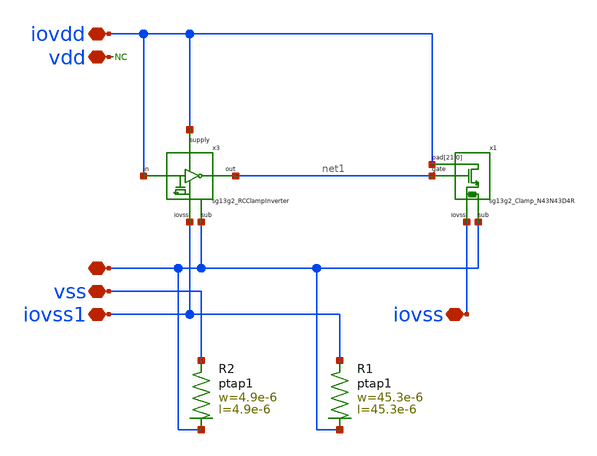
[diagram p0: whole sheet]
** sch_path: MSPHY6034-main/dependencies/unic_cass_2025_team04_padring/xschem/openpdk-libraries/ihp-sg13g2/sg13g2_io/xschem/sg13g2_IOPadIOVdd.sch
**.subckt sg13g2_IOPadIOVdd iovdd vss vdd ! iovss1 iovss
*.iopin iovdd
*.iopin vss
*.iopin vdd
*.iopin !
*.iopin iovss1
*.iopin iovss
XR2 vss ! ptap1 R=22.47 w=4.9e-6 l=4.9e-6
* noconn vdd
XR1 iovss1 ! ptap1 R=438.8m w=45.3e-6 l=45.3e-6
x1 iovss iovdd iovdd iovdd iovdd iovdd iovdd iovdd iovdd iovdd iovdd iovdd iovdd iovdd iovdd iovdd
+ iovdd iovdd iovdd iovdd iovdd iovdd iovdd ! net1 sg13g2_Clamp_N43N43D4R
x3 iovdd iovss1 iovdd net1 ! sg13g2_RCClampInverter
**.ends

* expanding   symbol:  sg13g2_Clamp_N43N43D4R.sym # of pins=4
** sym_path: MSPHY6034-main/schematic/xschem/openpdk-libraries/ihp-sg13g2/sg13g2_io/xschem/sg13g2_Clamp_N43N43D4R.sym
** sch_path: MSPHY6034-main/schematic/xschem/openpdk-libraries/ihp-sg13g2/sg13g2_io/xschem/sg13g2_Clamp_N43N43D4R.sch
.subckt sg13g2_Clamp_N43N43D4R iovss pad[21] pad[20] pad[19] pad[18] pad[17] pad[16] pad[15] pad[14]
+ pad[13] pad[12] pad[11] pad[10] pad[9] pad[8] pad[7] pad[6] pad[5] pad[4] pad[3] pad[2] pad[1] pad[0] sub
+ gate
*.iopin iovss
*.iopin
*+ pad[21],pad[20],pad[19],pad[18],pad[17],pad[16],pad[15],pad[14],pad[13],pad[12],pad[11],pad[10],pad[9],pad[8],pad[7],pad[6],pad[5],pad[4],pad[3],pad[2],pad[1],pad[0]
*.iopin sub
*.iopin gate
XR1 iovss sub ptap1 R=9.999 w=8.1e-6 l=8.1e-6
XM1 pad[11] gate iovss sub sg13_hv_nmos w=35.2u l=0.6u ng=8 m=1 mm_ok=1
XM2 pad[12] gate iovss sub sg13_hv_nmos w=35.2u l=0.6u ng=8 m=1 mm_ok=1
XM3 pad[13] gate iovss sub sg13_hv_nmos w=35.2u l=0.6u ng=8 m=1 mm_ok=1
XM4 pad[14] gate iovss sub sg13_hv_nmos w=35.2u l=0.6u ng=8 m=1 mm_ok=1
XM5 pad[15] gate iovss sub sg13_hv_nmos w=35.2u l=0.6u ng=8 m=1 mm_ok=1
XM6 pad[16] gate iovss sub sg13_hv_nmos w=35.2u l=0.6u ng=8 m=1 mm_ok=1
XM7 pad[17] gate iovss sub sg13_hv_nmos w=35.2u l=0.6u ng=8 m=1 mm_ok=1
XM8 pad[18] gate iovss sub sg13_hv_nmos w=35.2u l=0.6u ng=8 m=1 mm_ok=1
XM9 pad[19] gate iovss sub sg13_hv_nmos w=35.2u l=0.6u ng=8 m=1 mm_ok=1
XM10 pad[20] gate iovss sub sg13_hv_nmos w=35.2u l=0.6u ng=8 m=1 mm_ok=1
XM11 pad[21] gate iovss sub sg13_hv_nmos w=17.6u l=0.6u ng=4 m=1 mm_ok=1
XD1 sub gate dantenna l=0.48u w=0.48u
XM12 pad[0] gate iovss sub sg13_hv_nmos w=35.2u l=0.6u ng=8 m=1 mm_ok=1
XM13 pad[1] gate iovss sub sg13_hv_nmos w=35.2u l=0.6u ng=8 m=1 mm_ok=1
XM14 pad[2] gate iovss sub sg13_hv_nmos w=35.2u l=0.6u ng=8 m=1 mm_ok=1
XM15 pad[3] gate iovss sub sg13_hv_nmos w=35.2u l=0.6u ng=8 m=1 mm_ok=1
XM16 pad[4] gate iovss sub sg13_hv_nmos w=35.2u l=0.6u ng=8 m=1 mm_ok=1
XM17 pad[5] gate iovss sub sg13_hv_nmos w=35.2u l=0.6u ng=8 m=1 mm_ok=1
XM18 pad[6] gate iovss sub sg13_hv_nmos w=35.2u l=0.6u ng=8 m=1 mm_ok=1
XM19 pad[7] gate iovss sub sg13_hv_nmos w=35.2u l=0.6u ng=8 m=1 mm_ok=1
XM20 pad[8] gate iovss sub sg13_hv_nmos w=35.2u l=0.6u ng=8 m=1 mm_ok=1
XM21 pad[9] gate iovss sub sg13_hv_nmos w=35.2u l=0.6u ng=8 m=1 mm_ok=1
XM22 pad[10] gate iovss sub sg13_hv_nmos w=35.2u l=0.6u ng=8 m=1 mm_ok=1
.ends


* expanding   symbol:  sg13g2_RCClampInverter.sym # of pins=5
** sym_path: MSPHY6034-main/schematic/xschem/openpdk-libraries/ihp-sg13g2/sg13g2_io/xschem/sg13g2_RCClampInverter.sym
** sch_path: MSPHY6034-main/schematic/xschem/openpdk-libraries/ihp-sg13g2/sg13g2_io/xschem/sg13g2_RCClampInverter.sch
.subckt sg13g2_RCClampInverter supply iovss in out sub
*.iopin supply
*.iopin iovss
*.iopin out
*.iopin in
*.iopin sub
XR1 iovss sub ptap1 R=9.57 w=8.315e-6 l=8.315e-6
XM1 iovss in iovss sub sg13_hv_nmos w=126u l=9.5u ng=14 m=1 mm_ok=1
XM2 out in iovss sub sg13_hv_nmos w=108u l=0.5u ng=12 m=1 mm_ok=1
XM3 out in supply supply sg13_hv_pmos w=350u l=0.5u ng=50 m=1 mm_ok=1
.ends

.end
